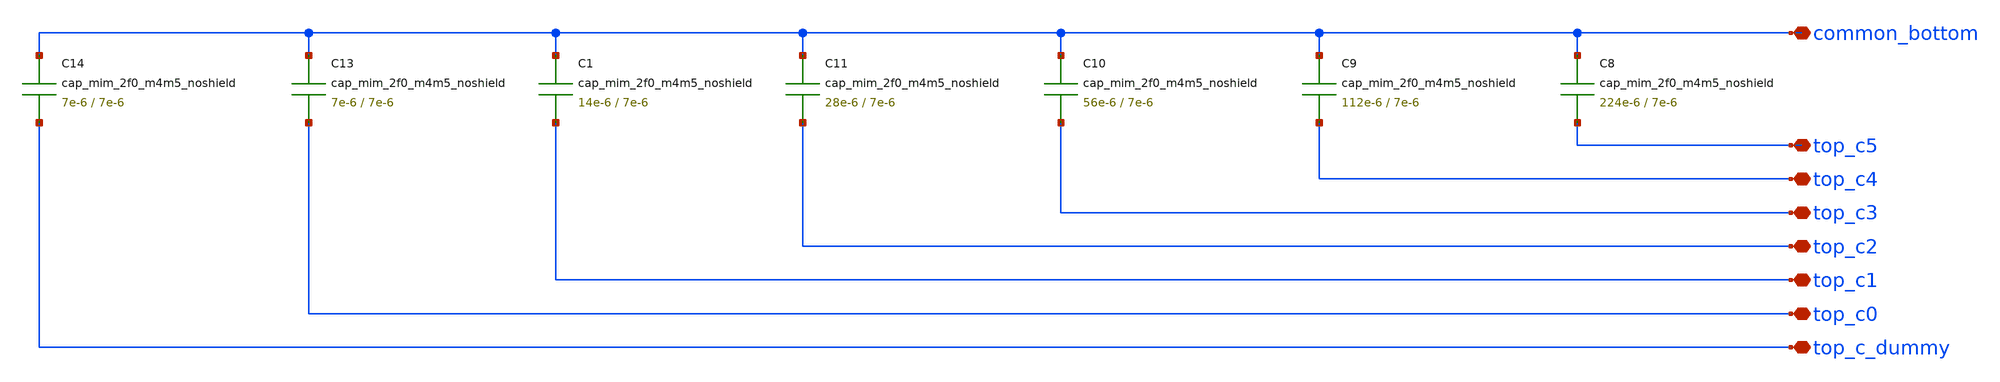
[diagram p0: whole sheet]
** sch_path: cdac/mim_cap_array_8x8/rev001/advanced_mimcap_array8x8_15step.sch
**.subckt advanced_mimcap_array8x8_15step common_bottom top_c5 top_c4 top_c3 top_c2 top_c1 top_c0
*+ top_c_dummy
*.iopin common_bottom
*.iopin top_c5
*.iopin top_c4
*.iopin top_c3
*.iopin top_c2
*.iopin top_c1
*.iopin top_c0
*.iopin top_c_dummy
C8 common_bottom top_c5 cap_mim_2f0_m4m5_noshield W=224e-6 L=7e-6
C9 common_bottom top_c4 cap_mim_2f0_m4m5_noshield W=112e-6 L=7e-6
C10 common_bottom top_c3 cap_mim_2f0_m4m5_noshield W=56e-6 L=7e-6
C11 common_bottom top_c2 cap_mim_2f0_m4m5_noshield W=28e-6 L=7e-6
C13 common_bottom top_c0 cap_mim_2f0_m4m5_noshield W=7e-6 L=7e-6
C14 common_bottom top_c_dummy cap_mim_2f0_m4m5_noshield W=7e-6 L=7e-6
C1 common_bottom top_c1 cap_mim_2f0_m4m5_noshield W=14e-6 L=7e-6
**.ends
.end
